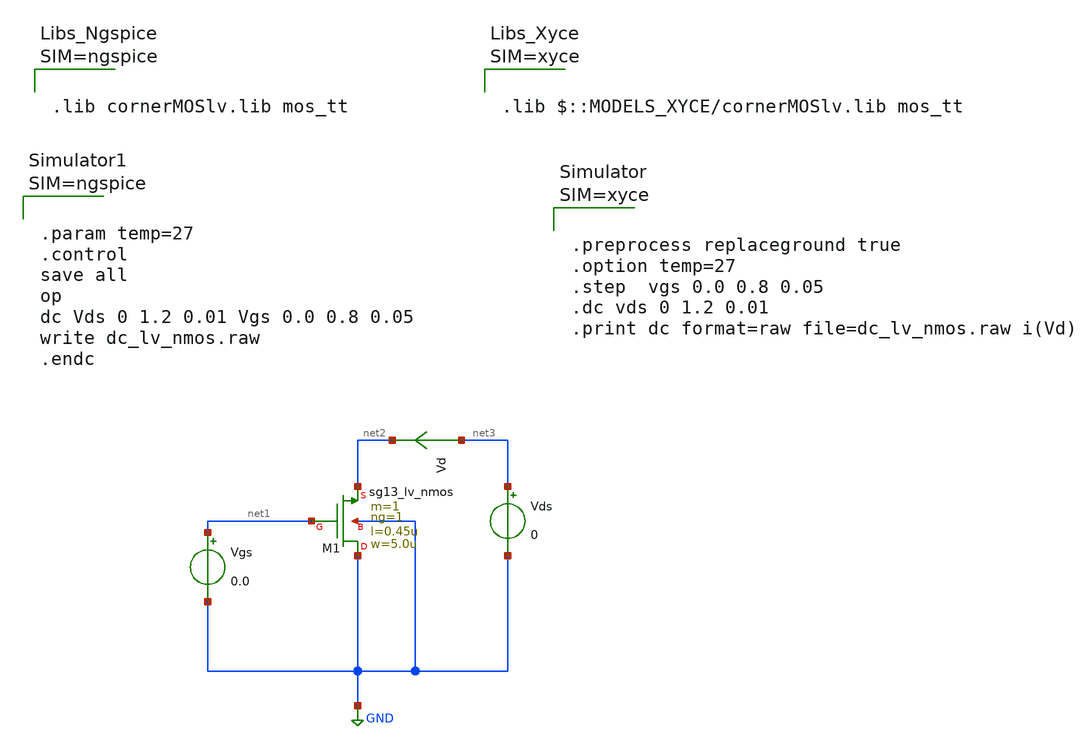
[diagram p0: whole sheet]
** sch_path: ihp-sg13g2/libs.tech/xschem/sg13g2_tests_xyce/dc_lv_nmos_xyce.sch
* Copyright 2023 IHP PDK Authors
**.subckt dc_lv_nmos_xyce
Vgs net1 GND 0.0
Vds net3 GND 0
Vd net3 net2 0
.save i(vd)
XM1 GND net1 net2 GND sg13_lv_nmos w=5.0u l=0.45u ng=1 m=1 mm_ok=1
**** begin user architecture code









.lib cornerMOSlv.lib mos_tt






.param temp=27
.control
save all
op
dc Vds 0 1.2 0.01 Vgs 0.0 0.8 0.05
write dc_lv_nmos.raw
.endc



**** end user architecture code
**.ends
.GLOBAL GND
.end
